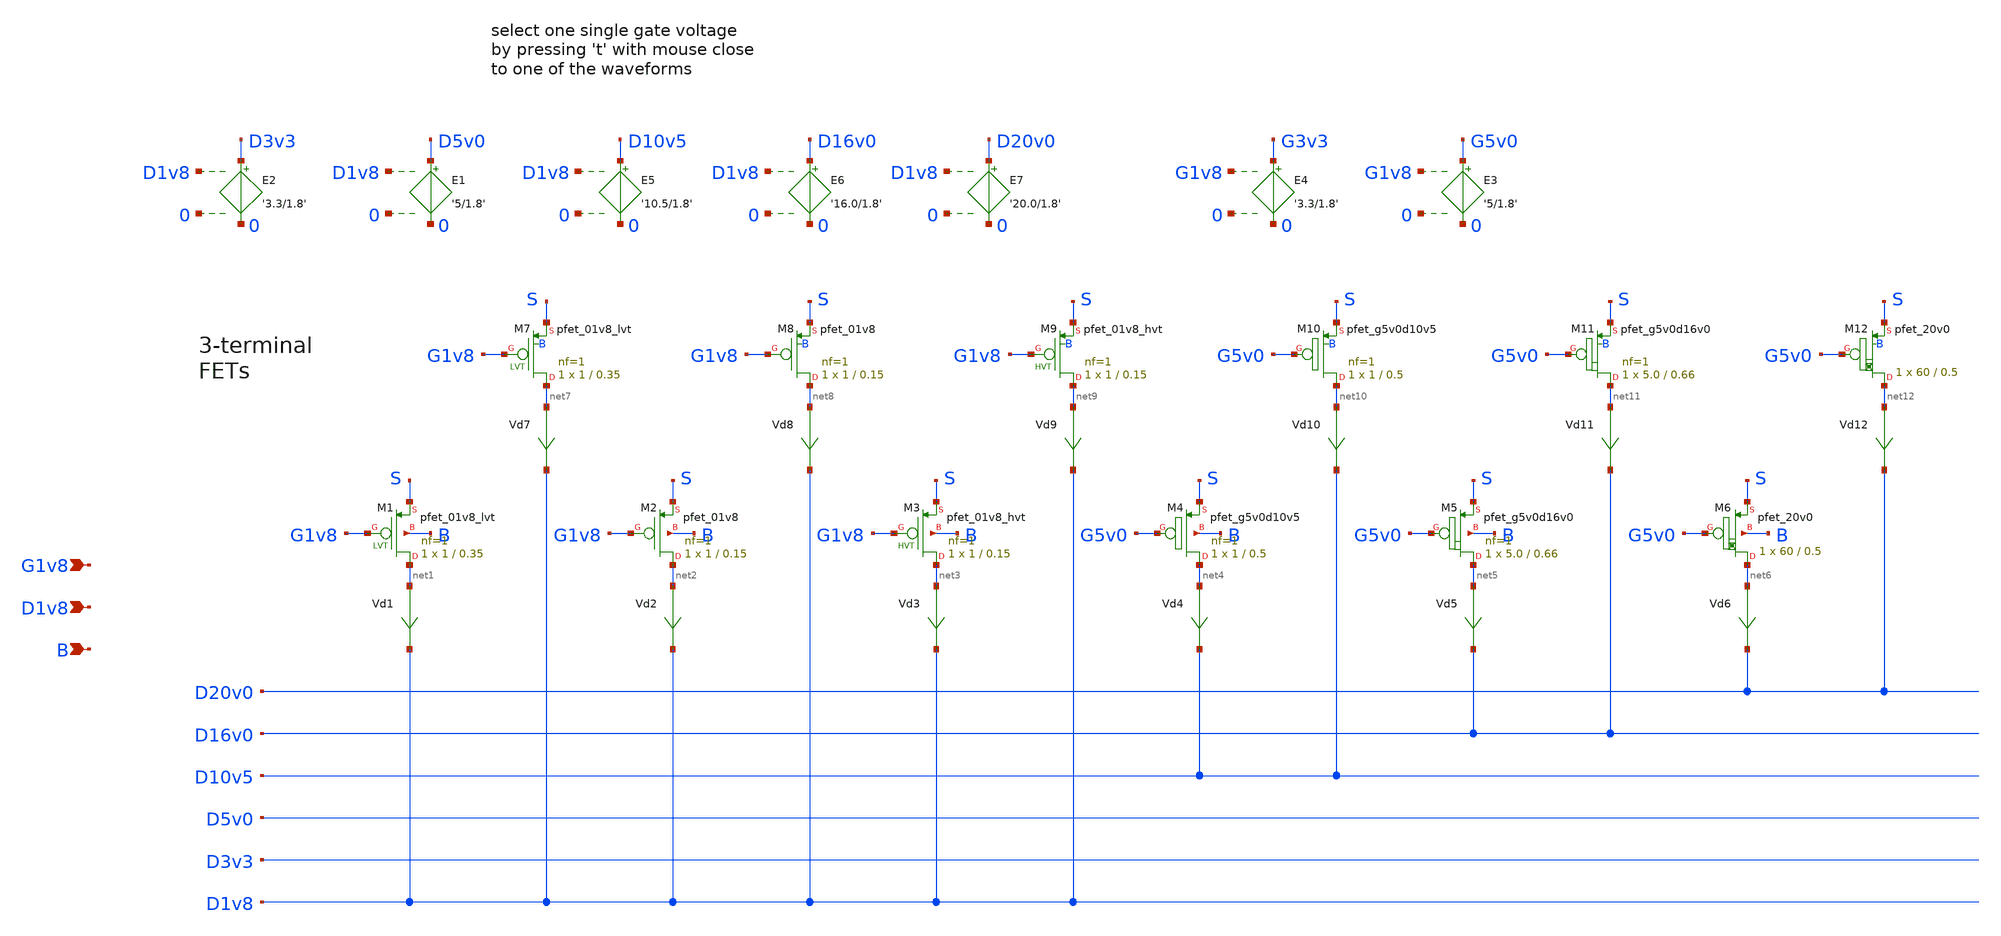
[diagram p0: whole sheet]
** sch_path: sky130A/xschem_libs/sky130_tests_ase/test_pmos/schematic/test_pmos.sch
* Copyright 2021 Stefan Frederik Schippers
* Licensed under the Apache License, Version 2.0 (the "License");
* you may not use this file except in compliance with the License.
* You may obtain a copy of the License at
* https://www.apache.org/licenses/LICENSE-2.0
* Unless required by applicable law or agreed to in writing, software
* distributed under the License is distributed on an "AS IS" BASIS,
* WITHOUT WARRANTIES OR CONDITIONS OF ANY KIND, either express or implied.
* See the License for the specific language governing permissions and
* limitations under the License.
**.subckt test_pmos G1v8 D1v8 B
*.ipin G1v8
*.ipin D1v8
*.ipin B
Vd1 net1 D1v8 0
.save i(vd1)
Vd2 net2 D1v8 0
.save i(vd2)
E1 D5v0 0 D1v8 0 '5/1.8'
E2 D3v3 0 D1v8 0 '3.3/1.8'
E3 G5v0 0 G1v8 0 '5/1.8'
E4 G3v3 0 G1v8 0 '3.3/1.8'
E5 D10v5 0 D1v8 0 '10.5/1.8'
Vd3 net3 D1v8 0
.save i(vd3)
XM3 net3 G1v8 S B sky130_fd_pr__pfet_01v8_hvt L=0.15 W=1 nf=1 ad='int((1 + 1)/2) * 1 / 1 * 0.29' as='int((1 + 2)/2) * 1 / 1 * 0.29'
+ pd='2*int((1 + 1)/2) * (1 / 1 + 0.29)' ps='2*int((1 + 2)/2) * (1 / 1 + 0.29)' nrd='0.29 / 1 ' nrs='0.29 / 1 '
+ sa=0 sb=0 sd=0 mult=1 m=1
Vd4 net4 D10v5 0
.save i(vd4)
XM4 net4 G5v0 S B sky130_fd_pr__pfet_g5v0d10v5 L=0.5 W=1 nf=1 ad='int((1 + 1)/2) * 1 / 1 * 0.29' as='int((1 + 2)/2) * 1 / 1 * 0.29'
+ pd='2*int((1 + 1)/2) * (1 / 1 + 0.29)' ps='2*int((1 + 2)/2) * (1 / 1 + 0.29)' nrd='0.29 / 1 ' nrs='0.29 / 1 '
+ sa=0 sb=0 sd=0 mult=1 m=1
XM1 net1 G1v8 S B sky130_fd_pr__pfet_01v8_lvt L=0.35 W=1 nf=1 ad='int((1 + 1)/2) * 1 / 1 * 0.29' as='int((1 + 2)/2) * 1 / 1 * 0.29'
+ pd='2*int((1 + 1)/2) * (1 / 1 + 0.29)' ps='2*int((1 + 2)/2) * (1 / 1 + 0.29)' nrd='0.29 / 1 ' nrs='0.29 / 1 '
+ sa=0 sb=0 sd=0 mult=1 m=1
XM2 net2 G1v8 S B sky130_fd_pr__pfet_01v8 L=0.15 W=1 nf=1 ad='int((nf+1)/2) * W/nf * 0.29' as='int((nf+2)/2) * W/nf * 0.29'
+ pd='2*int((nf+1)/2) * (W/nf + 0.29)' ps='2*int((nf+2)/2) * (W/nf + 0.29)' nrd='0.29 / W' nrs='0.29 / W'
+ sa=0 sb=0 sd=0 mult=1 m=1
Vd5 net5 D16v0 0
.save i(vd5)
XM5 net5 G5v0 S B sky130_fd_pr__pfet_g5v0d16v0 L=0.66 W=5.0 nf=1 ad='int((nf+1)/2) * W/nf * 0.29' as='int((nf+2)/2) * W/nf * 0.29'
+ pd='2*int((nf+1)/2) * (W/nf + 0.29)' ps='2*int((nf+2)/2) * (W/nf + 0.29)' nrd='0.29 / W' nrs='0.29 / W'
+ sa=0 sb=0 sd=0 mult=1 m=1
E6 D16v0 0 D1v8 0 '16.0/1.8'
E7 D20v0 0 D1v8 0 '20.0/1.8'
XM6 net6 G5v0 S B sky130_fd_pr__pfet_20v0 L=0.5 W=60 m=1
Vd6 net6 D20v0 0
.save i(vd6)
Vd7 net7 D1v8 0
.save i(vd7)
Vd8 net8 D1v8 0
.save i(vd8)
Vd9 net9 D1v8 0
.save i(vd9)
XM9 net9 G1v8 S B sky130_fd_pr__pfet_01v8_hvt L=0.15 W=1 nf=1 ad='int((1 + 1)/2) * 1 / 1 * 0.29' as='int((1 + 2)/2) * 1 / 1 * 0.29'
+ pd='2*int((1 + 1)/2) * (1 / 1 + 0.29)' ps='2*int((1 + 2)/2) * (1 / 1 + 0.29)' nrd='0.29 / 1 ' nrs='0.29 / 1 '
+ sa=0 sb=0 sd=0 mult=1 m=1
Vd10 net10 D10v5 0
.save i(vd10)
XM10 net10 G5v0 S B sky130_fd_pr__pfet_g5v0d10v5 L=0.5 W=1 nf=1 ad='int((nf+1)/2) * W/nf * 0.29' as='int((nf+2)/2) * W/nf * 0.29'
+ pd='2*int((nf+1)/2) * (W/nf + 0.29)' ps='2*int((nf+2)/2) * (W/nf + 0.29)' nrd='0.29 / W' nrs='0.29 / W'
+ sa=0 sb=0 sd=0 mult=1 m=1
XM7 net7 G1v8 S B sky130_fd_pr__pfet_01v8_lvt L=0.35 W=1 nf=1 ad='int((1 + 1)/2) * 1 / 1 * 0.29' as='int((1 + 2)/2) * 1 / 1 * 0.29'
+ pd='2*int((1 + 1)/2) * (1 / 1 + 0.29)' ps='2*int((1 + 2)/2) * (1 / 1 + 0.29)' nrd='0.29 / 1 ' nrs='0.29 / 1 '
+ sa=0 sb=0 sd=0 mult=1 m=1
XM8 net8 G1v8 S B sky130_fd_pr__pfet_01v8 L=0.15 W=1 nf=1 ad='int((1 + 1)/2) * 1 / 1 * 0.29' as='int((1 + 2)/2) * 1 / 1 * 0.29'
+ pd='2*int((1 + 1)/2) * (1 / 1 + 0.29)' ps='2*int((1 + 2)/2) * (1 / 1 + 0.29)' nrd='0.29 / 1 ' nrs='0.29 / 1 '
+ sa=0 sb=0 sd=0 mult=1 m=1
Vd11 net11 D16v0 0
.save i(vd11)
XM11 net11 G5v0 S B sky130_fd_pr__pfet_g5v0d16v0 L=0.66 W=5.0 nf=1 ad='int((1 + 1)/2) * 5.0 / 1 * 0.29'
+ as='int((1 + 2)/2) * 5.0 / 1 * 0.29' pd='2*int((1 + 1)/2) * (5.0 / 1 + 0.29)' ps='2*int((1 + 2)/2) * (5.0 / 1 + 0.29)'
+ nrd='0.29 / 5.0 ' nrs='0.29 / 5.0 ' sa=0 sb=0 sd=0 mult=1 m=1
XM12 net12 G5v0 S B sky130_fd_pr__pfet_20v0 L=0.5 W=60 m=1
Vd12 net12 D20v0 0
.save i(vd12)
**** begin user architecture code


.opton wnflag=1
vg G1v8 0 -1.8
vs s 0 0
vd D1v8 0 -1.8
vb b 0 0


**** end user architecture code
**.ends
.end
